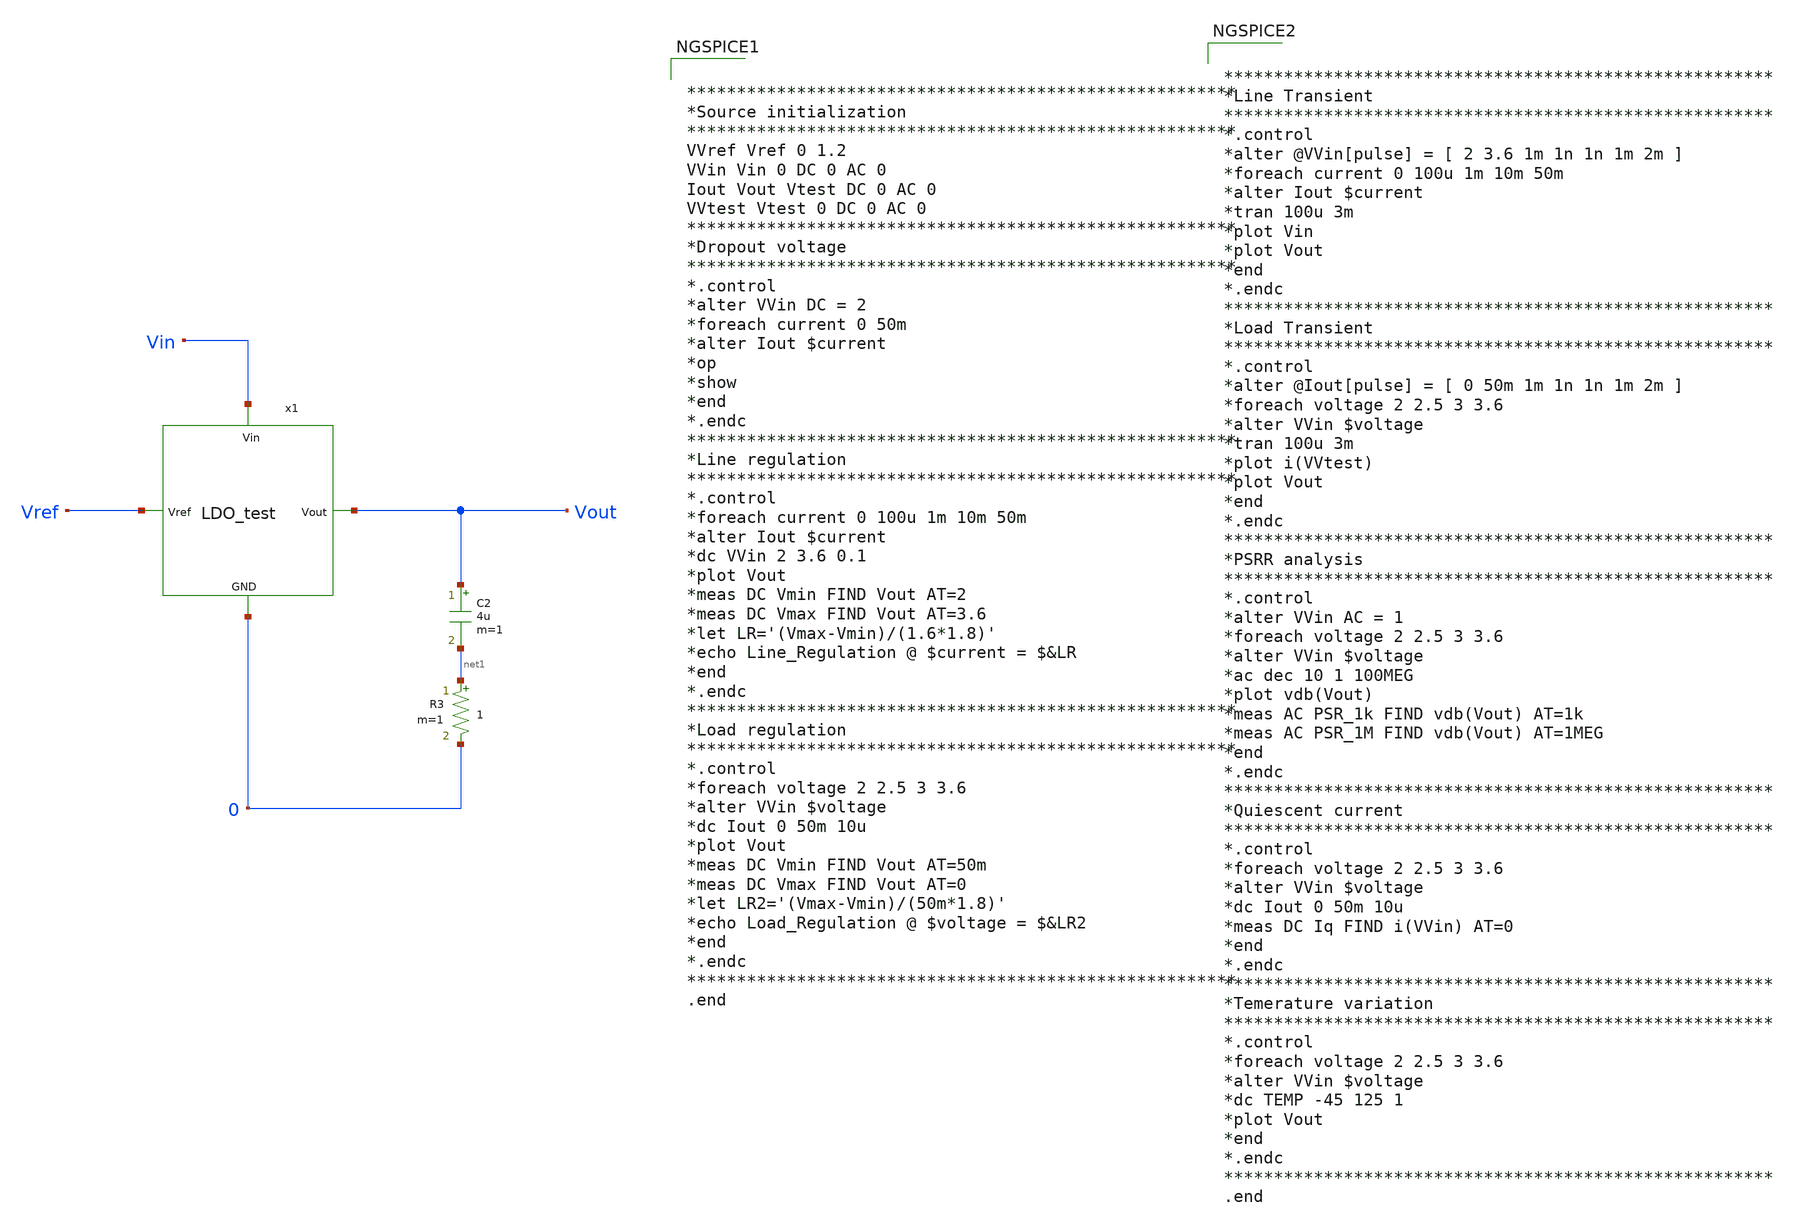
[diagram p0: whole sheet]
** sch_path: Analog_Blocks/LDO/Testbench/LDO_test_TB.sch
**.subckt LDO_test_TB
C2 Vout net1 4u m=1
R3 net1 0 1 m=1
x1 Vin Vref Vout 0 LDO_test
**** begin user architecture code


*******************************************************
*Source initialization
*******************************************************
VVref Vref 0 1.2
VVin Vin 0 DC 0 AC 0
Iout Vout Vtest DC 0 AC 0
VVtest Vtest 0 DC 0 AC 0
*******************************************************
*Dropout voltage
*******************************************************
*.control
*alter VVin DC = 2
*foreach current 0 50m
*alter Iout $current
*op
*show
*end
*.endc
*******************************************************
*Line regulation
*******************************************************
*.control
*foreach current 0 100u 1m 10m 50m
*alter Iout $current
*dc VVin 2 3.6 0.1
*plot Vout
*meas DC Vmin FIND Vout AT=2
*meas DC Vmax FIND Vout AT=3.6
*let LR='(Vmax-Vmin)/(1.6*1.8)'
*echo Line_Regulation @ $current = $&LR
*end
*.endc
*******************************************************
*Load regulation
*******************************************************
*.control
*foreach voltage 2 2.5 3 3.6
*alter VVin $voltage
*dc Iout 0 50m 10u
*plot Vout
*meas DC Vmin FIND Vout AT=50m
*meas DC Vmax FIND Vout AT=0
*let LR2='(Vmax-Vmin)/(50m*1.8)'
*echo Load_Regulation @ $voltage = $&LR2
*end
*.endc
*******************************************************
.end




.param mc_mm_switch=0
.param mc_pr_switch=0
.include ~/mabrains/Analog_blocks/models/sky130A/libs.ref/sky130_fd_pr/spice/sky130_fd_pr__nfet_01v8__sf.corner.spice
.include ~/mabrains/Analog_blocks/models/sky130A/libs.ref/sky130_fd_pr/spice/sky130_fd_pr__nfet_01v8_lvt__sf.corner.spice
.include ~/mabrains/Analog_blocks/models/sky130A/libs.ref/sky130_fd_pr/spice/sky130_fd_pr__pfet_01v8__sf.corner.spice
.include ~/mabrains/Analog_blocks/models/sky130A/libs.ref/sky130_fd_pr/spice/sky130_fd_pr__nfet_03v3_nvt__sf.corner.spice
.include ~/mabrains/Analog_blocks/models/sky130A/libs.ref/sky130_fd_pr/spice/sky130_fd_pr__nfet_05v0_nvt__sf.corner.spice
.include ~/mabrains/Analog_blocks/models/sky130A/libs.ref/sky130_fd_pr/spice/sky130_fd_pr__esd_nfet_01v8__sf.corner.spice
.include ~/mabrains/Analog_blocks/models/sky130A/libs.ref/sky130_fd_pr/spice/sky130_fd_pr__pfet_01v8_lvt__sf.corner.spice
.include ~/mabrains/Analog_blocks/models/sky130A/libs.ref/sky130_fd_pr/spice/sky130_fd_pr__pfet_01v8_hvt__sf.corner.spice
.include ~/mabrains/Analog_blocks/models/sky130A/libs.ref/sky130_fd_pr/spice/sky130_fd_pr__esd_pfet_g5v0d10v5__sf.corner.spice
.include ~/mabrains/Analog_blocks/models/sky130A/libs.ref/sky130_fd_pr/spice/sky130_fd_pr__pfet_g5v0d10v5__sf.corner.spice
.include ~/mabrains/Analog_blocks/models/sky130A/libs.ref/sky130_fd_pr/spice/sky130_fd_pr__pfet_g5v0d16v0__sf.corner.spice
.include ~/mabrains/Analog_blocks/models/sky130A/libs.ref/sky130_fd_pr/spice/sky130_fd_pr__nfet_g5v0d10v5__sf.corner.spice
.include ~/mabrains/Analog_blocks/models/sky130A/libs.ref/sky130_fd_pr/spice/sky130_fd_pr__nfet_g5v0d16v0__sf_discrete.corner.spice
.include ~/mabrains/Analog_blocks/models/sky130A/libs.ref/sky130_fd_pr/spice/sky130_fd_pr__esd_nfet_g5v0d10v5__sf.corner.spice
.include ~/mabrains/Analog_blocks/models/sky130A/libs.ref/sky130_fd_pr/spice/sky130_fd_pr__pfet_20v0__sf_discrete.corner.spice
.include ~/mabrains/Analog_blocks/models/sky130A/libs.ref/sky130_fd_pr/spice/sky130_fd_pr__nfet_20v0__sf_discrete.corner.spice
.include ~/mabrains/Analog_blocks/models/sky130A/libs.tech/ngspice/corners/sf/nonfet.spice
* Mismatch parameters
.include ~/mabrains/Analog_blocks/models/sky130A/libs.ref/sky130_fd_pr/spice/sky130_fd_pr__nfet_01v8__mismatch.corner.spice
.include ~/mabrains/Analog_blocks/models/sky130A/libs.ref/sky130_fd_pr/spice/sky130_fd_pr__pfet_01v8__mismatch.corner.spice
.include ~/mabrains/Analog_blocks/models/sky130A/libs.ref/sky130_fd_pr/spice/sky130_fd_pr__nfet_01v8_lvt__mismatch.corner.spice
.include ~/mabrains/Analog_blocks/models/sky130A/libs.ref/sky130_fd_pr/spice/sky130_fd_pr__pfet_01v8_lvt__mismatch.corner.spice
.include ~/mabrains/Analog_blocks/models/sky130A/libs.ref/sky130_fd_pr/spice/sky130_fd_pr__pfet_01v8_hvt__mismatch.corner.spice
.include ~/mabrains/Analog_blocks/models/sky130A/libs.ref/sky130_fd_pr/spice/sky130_fd_pr__nfet_g5v0d10v5__mismatch.corner.spice
.include ~/mabrains/Analog_blocks/models/sky130A/libs.ref/sky130_fd_pr/spice/sky130_fd_pr__pfet_g5v0d10v5__mismatch.corner.spice
.include ~/mabrains/Analog_blocks/models/sky130A/libs.ref/sky130_fd_pr/spice/sky130_fd_pr__nfet_05v0_nvt__mismatch.corner.spice
.include ~/mabrains/Analog_blocks/models/sky130A/libs.ref/sky130_fd_pr/spice/sky130_fd_pr__nfet_03v3_nvt__mismatch.corner.spice
* Resistor/Capacitor
.include ~/mabrains/Analog_blocks/models/sky130A/libs.tech/ngspice/r+c/res_typical__cap_typical.spice
.include ~/mabrains/Analog_blocks/models/sky130A/libs.tech/ngspice/r+c/res_typical__cap_typical__lin.spice
* Special cells
.include ~/mabrains/Analog_blocks/models/sky130A/libs.tech/ngspice/corners/sf/specialized_cells.spice
* All models
.include ~/mabrains/Analog_blocks/models/sky130A/libs.tech/ngspice/all.spice
* Corner
.include ~/mabrains/Analog_blocks/models/sky130A/libs.tech/ngspice/corners/sf/rf.spice





*******************************************************
*Line Transient
*******************************************************
*.control
*alter @VVin[pulse] = [ 2 3.6 1m 1n 1n 1m 2m ]
*foreach current 0 100u 1m 10m 50m
*alter Iout $current
*tran 100u 3m
*plot Vin
*plot Vout
*end
*.endc
*******************************************************
*Load Transient
*******************************************************
*.control
*alter @Iout[pulse] = [ 0 50m 1m 1n 1n 1m 2m ]
*foreach voltage 2 2.5 3 3.6
*alter VVin $voltage
*tran 100u 3m
*plot i(VVtest)
*plot Vout
*end
*.endc
*******************************************************
*PSRR analysis
*******************************************************
*.control
*alter VVin AC = 1
*foreach voltage 2 2.5 3 3.6
*alter VVin $voltage
*ac dec 10 1 100MEG
*plot vdb(Vout)
*meas AC PSR_1k FIND vdb(Vout) AT=1k
*meas AC PSR_1M FIND vdb(Vout) AT=1MEG
*end
*.endc
*******************************************************
*Quiescent current
*******************************************************
*.control
*foreach voltage 2 2.5 3 3.6
*alter VVin $voltage
*dc Iout 0 50m 10u
*meas DC Iq FIND i(VVin) AT=0
*end
*.endc
*******************************************************
*Temerature variation
*******************************************************
*.control
*foreach voltage 2 2.5 3 3.6
*alter VVin $voltage
*dc TEMP -45 125 1
*plot Vout
*end
*.endc
*******************************************************
.end


**** end user architecture code
**.ends
.end
